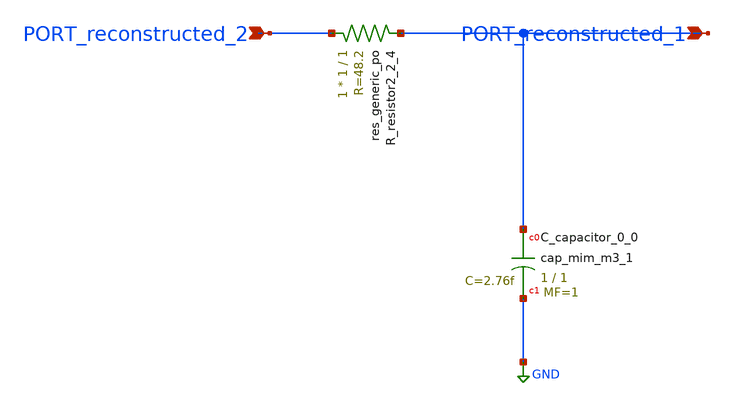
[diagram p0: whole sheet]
** sch_path: schematics/AMSNet/784.sch
**.subckt 784 PORT_reconstructed_1 PORT_reconstructed_2
*.ipin PORT_reconstructed_1
*.ipin PORT_reconstructed_2
XC_capacitor_0_0 PORT_reconstructed_1 GND sky130_fd_pr__cap_mim_m3_1 W=1 L=1 MF=1 m=1
XR_resistor2_2_4 PORT_reconstructed_2 PORT_reconstructed_1 sky130_fd_pr__res_generic_po W=1 L=1 m=1
**.ends
.GLOBAL GND
.end
